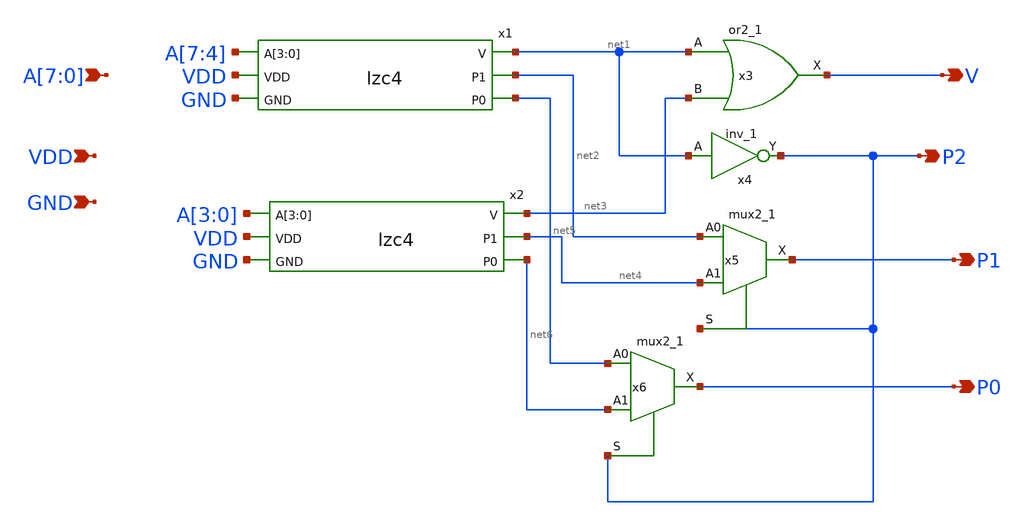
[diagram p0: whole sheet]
** sch_path: frontend/xschem/lzc8.sch
**.subckt lzc8 V P2 P1 P0 VDD GND A[7],A[6],A[5],A[4],A[3],A[2],A[1],A[0]
*.opin V
*.opin P2
*.opin P1
*.opin P0
*.ipin VDD
*.ipin GND
*.ipin A[7],A[6],A[5],A[4],A[3],A[2],A[1],A[0]
x1 A[7] A[6] A[5] A[4] net1 VDD net2 GND net5 lzc4
x2 A[3] A[2] A[1] A[0] net3 VDD net4 GND net6 lzc4
x3 net1 net3 GND GND VDD VDD V sky130_fd_sc_hd__or2_1
x4 net1 GND GND VDD VDD P2 sky130_fd_sc_hd__inv_1
x5 net2 net4 P2 GND GND VDD VDD P1 sky130_fd_sc_hd__mux2_1
x6 net5 net6 P2 GND GND VDD VDD P0 sky130_fd_sc_hd__mux2_1
**.ends

* expanding   symbol:  lzc4.sym # of pins=6
** sym_path: frontend/xschem/lzc4.sym
** sch_path: frontend/xschem/lzc4.sch
.subckt lzc4 A[3] A[2] A[1] A[0] V VDD P1 GND P0
*.ipin A[3],A[2],A[1],A[0]
*.opin V
*.opin P1
*.opin P0
*.ipin VDD
*.ipin GND
x1 A[3] net1 A[2] VDD net3 GND lzc2
x2 A[1] net2 A[0] VDD net4 GND lzc2
x3 net1 net2 GND GND VDD VDD V sky130_fd_sc_hd__or2_1
x4 net1 GND GND VDD VDD P1 sky130_fd_sc_hd__inv_1
x5 net3 net4 P1 GND GND VDD VDD P0 sky130_fd_sc_hd__mux2_1
.ends


* expanding   symbol:  lzc2.sym # of pins=6
** sym_path: frontend/xschem/lzc2.sym
** sch_path: frontend/xschem/lzc2.sch
.subckt lzc2 HI V LO VDD P GND
*.ipin HI
*.ipin LO
*.opin V
*.opin P
*.ipin VDD
*.ipin GND
x1 HI LO GND GND VDD VDD V sky130_fd_sc_hd__or2_1
x2 HI GND GND VDD VDD P sky130_fd_sc_hd__inv_1
.ends

.end
